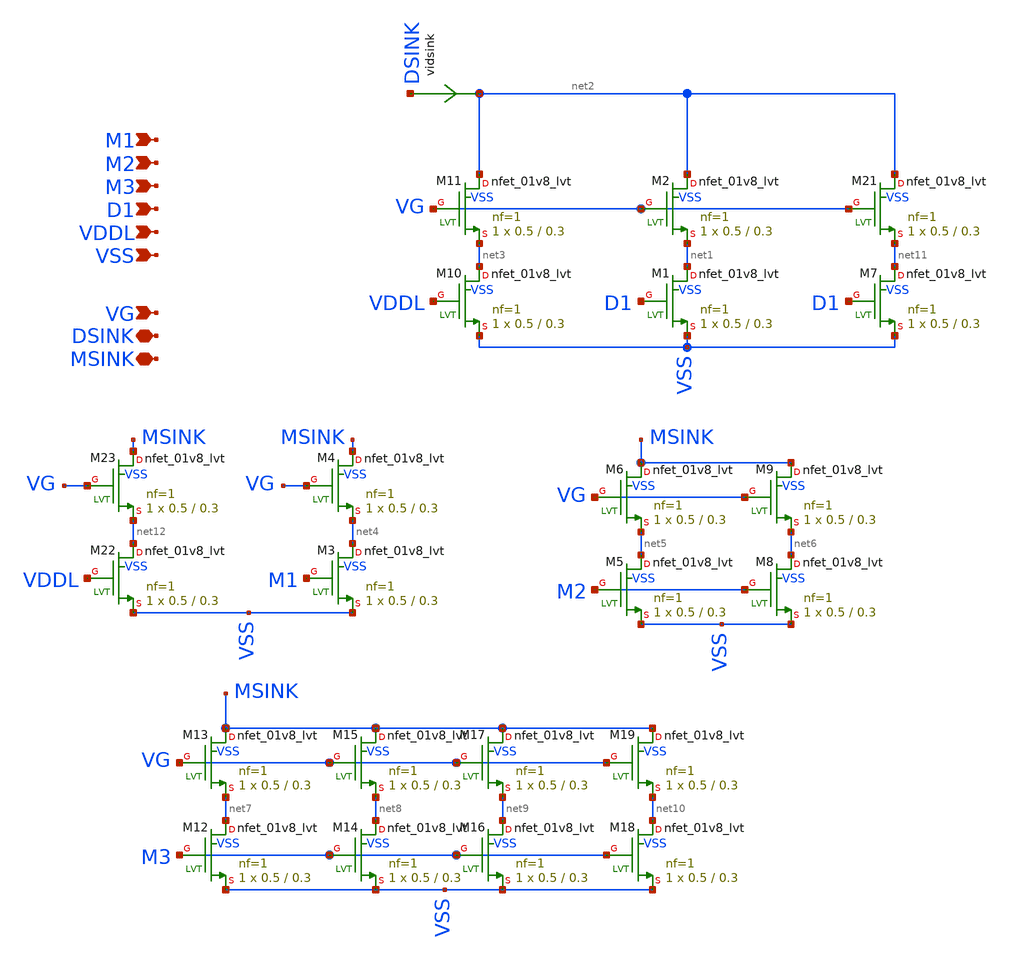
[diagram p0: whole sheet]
** sch_path: xschem/cmirror_adj1.sch
**.subckt cmirror_adj1 VSS VG VDDL MSINK M3 M2 M1 DSINK D1
*.ipin VSS
*.ipin VG
*.ipin VDDL
*.iopin MSINK
*.ipin M3
*.ipin M2
*.ipin M1
*.iopin DSINK
*.ipin D1
XM1 net1 D1 VSS VSS sky130_fd_pr__nfet_01v8_lvt L=0.3 W=0.5 nf=1 ad='int((nf+1)/2) * W/nf * 0.29' as='int((nf+2)/2) * W/nf * 0.29'
+ pd='2*int((nf+1)/2) * (W/nf + 0.29)' ps='2*int((nf+2)/2) * (W/nf + 0.29)' nrd='0.29 / W' nrs='0.29 / W'
+ sa=0 sb=0 sd=0 mult=1 m=1
XM2 net2 VG net1 VSS sky130_fd_pr__nfet_01v8_lvt L=0.3 W=0.5 nf=1 ad='int((nf+1)/2) * W/nf * 0.29' as='int((nf+2)/2) * W/nf * 0.29'
+ pd='2*int((nf+1)/2) * (W/nf + 0.29)' ps='2*int((nf+2)/2) * (W/nf + 0.29)' nrd='0.29 / W' nrs='0.29 / W'
+ sa=0 sb=0 sd=0 mult=1 m=1
XM10 net3 VDDL VSS VSS sky130_fd_pr__nfet_01v8_lvt L=0.3 W=0.5 nf=1 ad='int((nf+1)/2) * W/nf * 0.29'
+ as='int((nf+2)/2) * W/nf * 0.29' pd='2*int((nf+1)/2) * (W/nf + 0.29)' ps='2*int((nf+2)/2) * (W/nf + 0.29)'
+ nrd='0.29 / W' nrs='0.29 / W' sa=0 sb=0 sd=0 mult=1 m=1
XM11 net2 VG net3 VSS sky130_fd_pr__nfet_01v8_lvt L=0.3 W=0.5 nf=1 ad='int((nf+1)/2) * W/nf * 0.29' as='int((nf+2)/2) * W/nf * 0.29'
+ pd='2*int((nf+1)/2) * (W/nf + 0.29)' ps='2*int((nf+2)/2) * (W/nf + 0.29)' nrd='0.29 / W' nrs='0.29 / W'
+ sa=0 sb=0 sd=0 mult=1 m=1
XM3 net4 M1 VSS VSS sky130_fd_pr__nfet_01v8_lvt L=0.3 W=0.5 nf=1 ad='int((nf+1)/2) * W/nf * 0.29' as='int((nf+2)/2) * W/nf * 0.29'
+ pd='2*int((nf+1)/2) * (W/nf + 0.29)' ps='2*int((nf+2)/2) * (W/nf + 0.29)' nrd='0.29 / W' nrs='0.29 / W'
+ sa=0 sb=0 sd=0 mult=1 m=1
XM4 MSINK VG net4 VSS sky130_fd_pr__nfet_01v8_lvt L=0.3 W=0.5 nf=1 ad='int((nf+1)/2) * W/nf * 0.29' as='int((nf+2)/2) * W/nf * 0.29'
+ pd='2*int((nf+1)/2) * (W/nf + 0.29)' ps='2*int((nf+2)/2) * (W/nf + 0.29)' nrd='0.29 / W' nrs='0.29 / W'
+ sa=0 sb=0 sd=0 mult=1 m=1
XM5 net5 M2 VSS VSS sky130_fd_pr__nfet_01v8_lvt L=0.3 W=0.5 nf=1 ad='int((nf+1)/2) * W/nf * 0.29' as='int((nf+2)/2) * W/nf * 0.29'
+ pd='2*int((nf+1)/2) * (W/nf + 0.29)' ps='2*int((nf+2)/2) * (W/nf + 0.29)' nrd='0.29 / W' nrs='0.29 / W'
+ sa=0 sb=0 sd=0 mult=1 m=1
XM6 MSINK VG net5 VSS sky130_fd_pr__nfet_01v8_lvt L=0.3 W=0.5 nf=1 ad='int((nf+1)/2) * W/nf * 0.29' as='int((nf+2)/2) * W/nf * 0.29'
+ pd='2*int((nf+1)/2) * (W/nf + 0.29)' ps='2*int((nf+2)/2) * (W/nf + 0.29)' nrd='0.29 / W' nrs='0.29 / W'
+ sa=0 sb=0 sd=0 mult=1 m=1
XM8 net6 M2 VSS VSS sky130_fd_pr__nfet_01v8_lvt L=0.3 W=0.5 nf=1 ad='int((nf+1)/2) * W/nf * 0.29' as='int((nf+2)/2) * W/nf * 0.29'
+ pd='2*int((nf+1)/2) * (W/nf + 0.29)' ps='2*int((nf+2)/2) * (W/nf + 0.29)' nrd='0.29 / W' nrs='0.29 / W'
+ sa=0 sb=0 sd=0 mult=1 m=1
XM9 MSINK VG net6 VSS sky130_fd_pr__nfet_01v8_lvt L=0.3 W=0.5 nf=1 ad='int((nf+1)/2) * W/nf * 0.29' as='int((nf+2)/2) * W/nf * 0.29'
+ pd='2*int((nf+1)/2) * (W/nf + 0.29)' ps='2*int((nf+2)/2) * (W/nf + 0.29)' nrd='0.29 / W' nrs='0.29 / W'
+ sa=0 sb=0 sd=0 mult=1 m=1
XM12 net7 M3 VSS VSS sky130_fd_pr__nfet_01v8_lvt L=0.3 W=0.5 nf=1 ad='int((nf+1)/2) * W/nf * 0.29' as='int((nf+2)/2) * W/nf * 0.29'
+ pd='2*int((nf+1)/2) * (W/nf + 0.29)' ps='2*int((nf+2)/2) * (W/nf + 0.29)' nrd='0.29 / W' nrs='0.29 / W'
+ sa=0 sb=0 sd=0 mult=1 m=1
XM13 MSINK VG net7 VSS sky130_fd_pr__nfet_01v8_lvt L=0.3 W=0.5 nf=1 ad='int((nf+1)/2) * W/nf * 0.29'
+ as='int((nf+2)/2) * W/nf * 0.29' pd='2*int((nf+1)/2) * (W/nf + 0.29)' ps='2*int((nf+2)/2) * (W/nf + 0.29)'
+ nrd='0.29 / W' nrs='0.29 / W' sa=0 sb=0 sd=0 mult=1 m=1
XM14 net8 M3 VSS VSS sky130_fd_pr__nfet_01v8_lvt L=0.3 W=0.5 nf=1 ad='int((nf+1)/2) * W/nf * 0.29' as='int((nf+2)/2) * W/nf * 0.29'
+ pd='2*int((nf+1)/2) * (W/nf + 0.29)' ps='2*int((nf+2)/2) * (W/nf + 0.29)' nrd='0.29 / W' nrs='0.29 / W'
+ sa=0 sb=0 sd=0 mult=1 m=1
XM15 MSINK VG net8 VSS sky130_fd_pr__nfet_01v8_lvt L=0.3 W=0.5 nf=1 ad='int((nf+1)/2) * W/nf * 0.29'
+ as='int((nf+2)/2) * W/nf * 0.29' pd='2*int((nf+1)/2) * (W/nf + 0.29)' ps='2*int((nf+2)/2) * (W/nf + 0.29)'
+ nrd='0.29 / W' nrs='0.29 / W' sa=0 sb=0 sd=0 mult=1 m=1
XM16 net9 M3 VSS VSS sky130_fd_pr__nfet_01v8_lvt L=0.3 W=0.5 nf=1 ad='int((nf+1)/2) * W/nf * 0.29' as='int((nf+2)/2) * W/nf * 0.29'
+ pd='2*int((nf+1)/2) * (W/nf + 0.29)' ps='2*int((nf+2)/2) * (W/nf + 0.29)' nrd='0.29 / W' nrs='0.29 / W'
+ sa=0 sb=0 sd=0 mult=1 m=1
XM17 MSINK VG net9 VSS sky130_fd_pr__nfet_01v8_lvt L=0.3 W=0.5 nf=1 ad='int((nf+1)/2) * W/nf * 0.29'
+ as='int((nf+2)/2) * W/nf * 0.29' pd='2*int((nf+1)/2) * (W/nf + 0.29)' ps='2*int((nf+2)/2) * (W/nf + 0.29)'
+ nrd='0.29 / W' nrs='0.29 / W' sa=0 sb=0 sd=0 mult=1 m=1
XM18 net10 M3 VSS VSS sky130_fd_pr__nfet_01v8_lvt L=0.3 W=0.5 nf=1 ad='int((nf+1)/2) * W/nf * 0.29' as='int((nf+2)/2) * W/nf * 0.29'
+ pd='2*int((nf+1)/2) * (W/nf + 0.29)' ps='2*int((nf+2)/2) * (W/nf + 0.29)' nrd='0.29 / W' nrs='0.29 / W'
+ sa=0 sb=0 sd=0 mult=1 m=1
XM19 MSINK VG net10 VSS sky130_fd_pr__nfet_01v8_lvt L=0.3 W=0.5 nf=1 ad='int((nf+1)/2) * W/nf * 0.29'
+ as='int((nf+2)/2) * W/nf * 0.29' pd='2*int((nf+1)/2) * (W/nf + 0.29)' ps='2*int((nf+2)/2) * (W/nf + 0.29)'
+ nrd='0.29 / W' nrs='0.29 / W' sa=0 sb=0 sd=0 mult=1 m=1
XM7 net11 D1 VSS VSS sky130_fd_pr__nfet_01v8_lvt L=0.3 W=0.5 nf=1 ad='int((nf+1)/2) * W/nf * 0.29' as='int((nf+2)/2) * W/nf * 0.29'
+ pd='2*int((nf+1)/2) * (W/nf + 0.29)' ps='2*int((nf+2)/2) * (W/nf + 0.29)' nrd='0.29 / W' nrs='0.29 / W'
+ sa=0 sb=0 sd=0 mult=1 m=1
XM21 net2 VG net11 VSS sky130_fd_pr__nfet_01v8_lvt L=0.3 W=0.5 nf=1 ad='int((nf+1)/2) * W/nf * 0.29'
+ as='int((nf+2)/2) * W/nf * 0.29' pd='2*int((nf+1)/2) * (W/nf + 0.29)' ps='2*int((nf+2)/2) * (W/nf + 0.29)'
+ nrd='0.29 / W' nrs='0.29 / W' sa=0 sb=0 sd=0 mult=1 m=1
XM22 net12 VDDL VSS VSS sky130_fd_pr__nfet_01v8_lvt L=0.3 W=0.5 nf=1 ad='int((nf+1)/2) * W/nf * 0.29'
+ as='int((nf+2)/2) * W/nf * 0.29' pd='2*int((nf+1)/2) * (W/nf + 0.29)' ps='2*int((nf+2)/2) * (W/nf + 0.29)'
+ nrd='0.29 / W' nrs='0.29 / W' sa=0 sb=0 sd=0 mult=1 m=1
XM23 MSINK VG net12 VSS sky130_fd_pr__nfet_01v8_lvt L=0.3 W=0.5 nf=1 ad='int((nf+1)/2) * W/nf * 0.29'
+ as='int((nf+2)/2) * W/nf * 0.29' pd='2*int((nf+1)/2) * (W/nf + 0.29)' ps='2*int((nf+2)/2) * (W/nf + 0.29)'
+ nrd='0.29 / W' nrs='0.29 / W' sa=0 sb=0 sd=0 mult=1 m=1
vidsink DSINK net2 0
.save i(vidsink)
**.ends
.end
